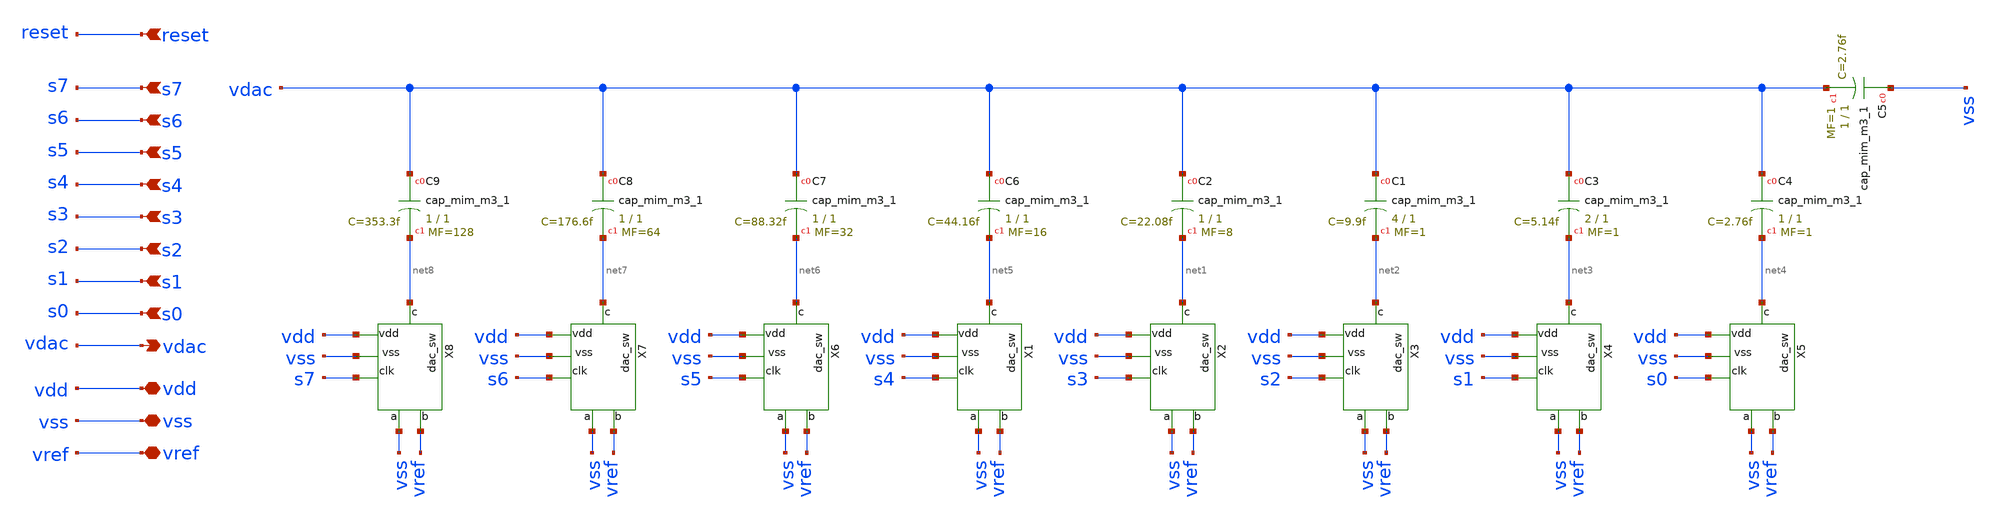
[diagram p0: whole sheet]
** sch_path: xschem/dac/dac.sch
**.subckt dac s7 s6 s5 s4 s3 s2 s1 s0 vdd vss vref vdac reset
*.ipin s7
*.ipin s6
*.ipin s5
*.ipin s4
*.ipin s3
*.ipin s2
*.ipin s1
*.ipin s0
*.iopin vdd
*.iopin vss
*.iopin vref
*.opin vdac
*.ipin reset
XC2 vdac net1 sky130_fd_pr__cap_mim_m3_1 W=1 L=1 MF=8 m=8
X2 net1 vref vss vdd s3 vss dac_sw
XC1 vdac net2 sky130_fd_pr__cap_mim_m3_1 W=4 L=1 MF=1 m=1
X3 net2 vref vss vdd s2 vss dac_sw
X4 net3 vref vss vdd s1 vss dac_sw
X5 net4 vref vss vdd s0 vss dac_sw
XC3 vdac net3 sky130_fd_pr__cap_mim_m3_1 W=2 L=1 MF=1 m=1
XC4 vdac net4 sky130_fd_pr__cap_mim_m3_1 W=1 L=1 MF=1 m=1
XC5 vss vdac sky130_fd_pr__cap_mim_m3_1 W=1 L=1 MF=1 m=1
XC6 vdac net5 sky130_fd_pr__cap_mim_m3_1 W=1 L=1 MF=16 m=16
X1 net5 vref vss vdd s4 vss dac_sw
XC7 vdac net6 sky130_fd_pr__cap_mim_m3_1 W=1 L=1 MF=32 m=32
X6 net6 vref vss vdd s5 vss dac_sw
XC8 vdac net7 sky130_fd_pr__cap_mim_m3_1 W=1 L=1 MF=64 m=64
X7 net7 vref vss vdd s6 vss dac_sw
XC9 vdac net8 sky130_fd_pr__cap_mim_m3_1 W=1 L=1 MF=128 m=128
X8 net8 vref vss vdd s7 vss dac_sw
**.ends

* expanding   symbol:  xschem/dac/dac_sw.sym # of pins=6
** sym_path: xschem/dac/dac_sw.sym
** sch_path: xschem/dac/dac_sw.sch
.subckt dac_sw c b vss vdd clk a
*.iopin vdd
*.iopin vss
*.ipin clk
*.iopin c
*.iopin a
*.iopin b
XM2 c clk b vss sky130_fd_pr__nfet_01v8 L=0.15 W=10 nf=1 ad='int((nf+1)/2) * W/nf * 0.29' as='int((nf+2)/2) * W/nf * 0.29'
+ pd='2*int((nf+1)/2) * (W/nf + 0.29)' ps='2*int((nf+2)/2) * (W/nf + 0.29)' nrd='0.29 / W' nrs='0.29 / W'
+ sa=0 sb=0 sd=0 mult=1 m=1
XM5 b net1 c vdd sky130_fd_pr__pfet_01v8 L=0.15 W=20 nf=1 ad='int((nf+1)/2) * W/nf * 0.29' as='int((nf+2)/2) * W/nf * 0.29'
+ pd='2*int((nf+1)/2) * (W/nf + 0.29)' ps='2*int((nf+2)/2) * (W/nf + 0.29)' nrd='0.29 / W' nrs='0.29 / W'
+ sa=0 sb=0 sd=0 mult=1 m=1
XM6 c net1 a vss sky130_fd_pr__nfet_01v8 L=0.15 W=10 nf=1 ad='int((nf+1)/2) * W/nf * 0.29' as='int((nf+2)/2) * W/nf * 0.29'
+ pd='2*int((nf+1)/2) * (W/nf + 0.29)' ps='2*int((nf+2)/2) * (W/nf + 0.29)' nrd='0.29 / W' nrs='0.29 / W'
+ sa=0 sb=0 sd=0 mult=1 m=1
XM7 a clk c vdd sky130_fd_pr__pfet_01v8 L=0.15 W=20 nf=1 ad='int((nf+1)/2) * W/nf * 0.29' as='int((nf+2)/2) * W/nf * 0.29'
+ pd='2*int((nf+1)/2) * (W/nf + 0.29)' ps='2*int((nf+2)/2) * (W/nf + 0.29)' nrd='0.29 / W' nrs='0.29 / W'
+ sa=0 sb=0 sd=0 mult=1 m=1
x1 clk vss vss vdd vdd net1 sky130_fd_sc_hd__inv_1
.ends

.end
